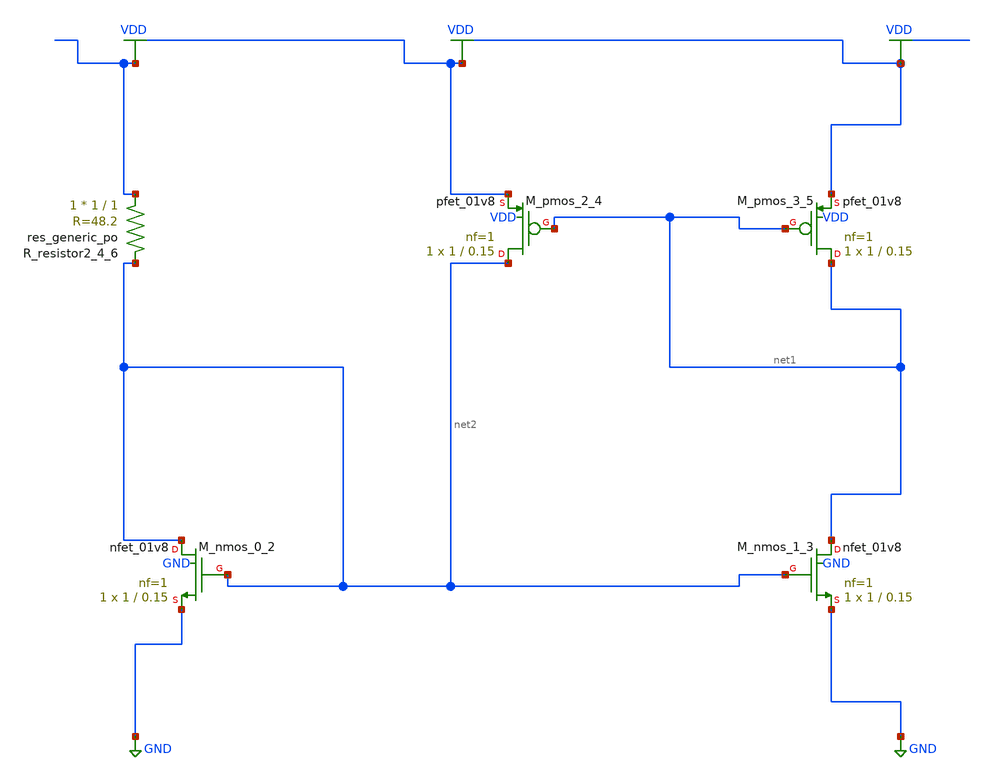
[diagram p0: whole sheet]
** sch_path: schematics/AMSNet/326.sch
**.subckt 326
XM_nmos_0_2 net2 net2 GND GND sky130_fd_pr__nfet_01v8 L=0.15 W=1 nf=1 ad='int((1 + 1)/2) * 1 / 1 * 0.29'
+ as='int((1 + 2)/2) * 1 / 1 * 0.29' pd='2*int((1 + 1)/2) * (1 / 1 + 0.29)' ps='2*int((1 + 2)/2) * (1 / 1 + 0.29)'
+ nrd='0.29 / 1 ' nrs='0.29 / 1 ' sa=0 sb=0 sd=0 mult=1 m=1
XM_nmos_1_3 net1 net2 GND GND sky130_fd_pr__nfet_01v8 L=0.15 W=1 nf=1 ad='int((1 + 1)/2) * 1 / 1 * 0.29'
+ as='int((1 + 2)/2) * 1 / 1 * 0.29' pd='2*int((1 + 1)/2) * (1 / 1 + 0.29)' ps='2*int((1 + 2)/2) * (1 / 1 + 0.29)'
+ nrd='0.29 / 1 ' nrs='0.29 / 1 ' sa=0 sb=0 sd=0 mult=1 m=1
XM_pmos_2_4 net2 net1 VDD VDD sky130_fd_pr__pfet_01v8 L=0.15 W=1 nf=1 ad='int((1 + 1)/2) * 1 / 1 * 0.29'
+ as='int((1 + 2)/2) * 1 / 1 * 0.29' pd='2*int((1 + 1)/2) * (1 / 1 + 0.29)' ps='2*int((1 + 2)/2) * (1 / 1 + 0.29)'
+ nrd='0.29 / 1 ' nrs='0.29 / 1 ' sa=0 sb=0 sd=0 mult=1 m=1
XM_pmos_3_5 net1 net1 VDD VDD sky130_fd_pr__pfet_01v8 L=0.15 W=1 nf=1 ad='int((1 + 1)/2) * 1 / 1 * 0.29'
+ as='int((1 + 2)/2) * 1 / 1 * 0.29' pd='2*int((1 + 1)/2) * (1 / 1 + 0.29)' ps='2*int((1 + 2)/2) * (1 / 1 + 0.29)'
+ nrd='0.29 / 1 ' nrs='0.29 / 1 ' sa=0 sb=0 sd=0 mult=1 m=1
XR_resistor2_4_6 VDD net2 sky130_fd_pr__res_generic_po W=1 L=1 m=1
**.ends
.GLOBAL GND
.GLOBAL VDD
.end
